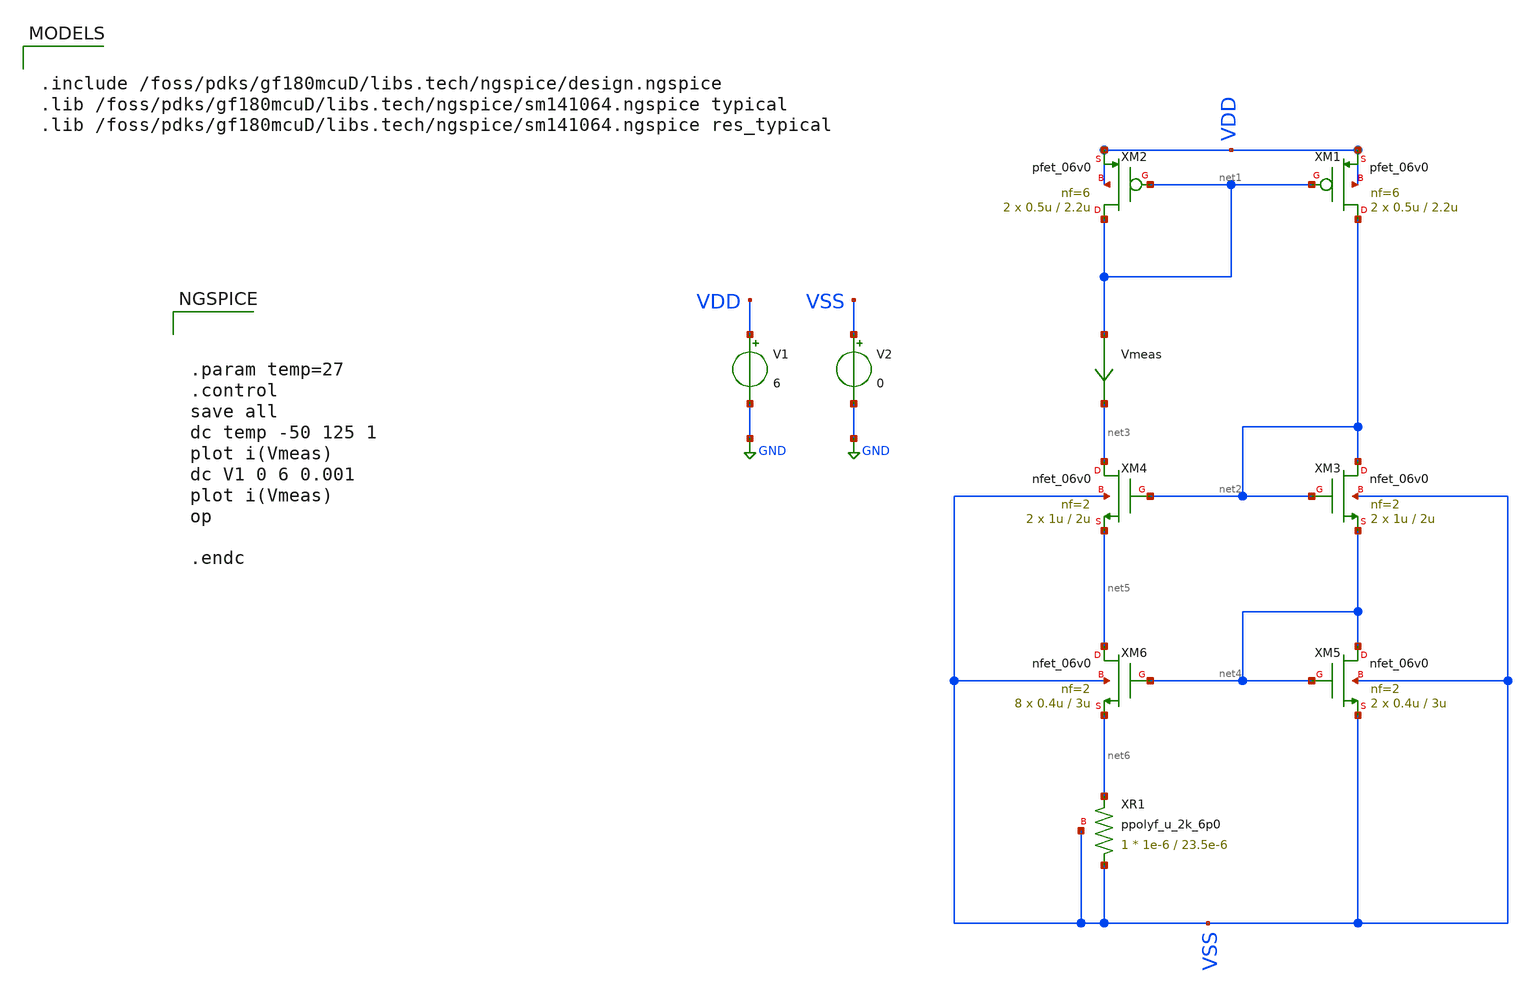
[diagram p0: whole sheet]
** sch_path: Learning/single_ended_amplifiers/VA001_series/Design_and_Analysis_of_Two-Stage_CMOS_Operational_Amplifier_for_Fluorescence_Signal_Processing_gf180mcu_6V/transcondutance/tb.sch
**.subckt tb
XM1 net2 net1 VDD VDD pfet_06v0 L=2.2u W=0.5u nf=6 ad='int((nf+1)/2) * W/nf * 0.18u' as='int((nf+2)/2) * W/nf * 0.18u'
+ pd='2*int((nf+1)/2) * (W/nf + 0.18u)' ps='2*int((nf+2)/2) * (W/nf + 0.18u)' nrd='0.18u / W' nrs='0.18u / W'
+ sa=0 sb=0 sd=0 m=2
XM2 net1 net1 VDD VDD pfet_06v0 L=2.2u W=0.5u nf=6 ad='int((nf+1)/2) * W/nf * 0.18u' as='int((nf+2)/2) * W/nf * 0.18u'
+ pd='2*int((nf+1)/2) * (W/nf + 0.18u)' ps='2*int((nf+2)/2) * (W/nf + 0.18u)' nrd='0.18u / W' nrs='0.18u / W'
+ sa=0 sb=0 sd=0 m=2
Vmeas net1 net3 0
.save i(vmeas)
V1 VDD GND 6
V2 VSS GND 0
XM3 net2 net2 net4 VSS nfet_06v0 L=2u W=1u nf=2 ad='int((nf+1)/2) * W/nf * 0.18u' as='int((nf+2)/2) * W/nf * 0.18u'
+ pd='2*int((nf+1)/2) * (W/nf + 0.18u)' ps='2*int((nf+2)/2) * (W/nf + 0.18u)' nrd='0.18u / W' nrs='0.18u / W'
+ sa=0 sb=0 sd=0 m=2
XM4 net3 net2 net5 VSS nfet_06v0 L=2u W=1u nf=2 ad='int((nf+1)/2) * W/nf * 0.18u' as='int((nf+2)/2) * W/nf * 0.18u'
+ pd='2*int((nf+1)/2) * (W/nf + 0.18u)' ps='2*int((nf+2)/2) * (W/nf + 0.18u)' nrd='0.18u / W' nrs='0.18u / W'
+ sa=0 sb=0 sd=0 m=2
XM6 net5 net4 net6 VSS nfet_06v0 L=3u W=0.4u nf=2 ad='int((nf+1)/2) * W/nf * 0.18u' as='int((nf+2)/2) * W/nf * 0.18u'
+ pd='2*int((nf+1)/2) * (W/nf + 0.18u)' ps='2*int((nf+2)/2) * (W/nf + 0.18u)' nrd='0.18u / W' nrs='0.18u / W'
+ sa=0 sb=0 sd=0 m=8
XR1 VSS net6 VSS ppolyf_u_2k_6p0 r_width=1e-6 r_length=23.5e-6 m=1
XM5 net4 net4 VSS VSS nfet_06v0 L=3u W=0.4u nf=2 ad='int((nf+1)/2) * W/nf * 0.18u' as='int((nf+2)/2) * W/nf * 0.18u'
+ pd='2*int((nf+1)/2) * (W/nf + 0.18u)' ps='2*int((nf+2)/2) * (W/nf + 0.18u)' nrd='0.18u / W' nrs='0.18u / W'
+ sa=0 sb=0 sd=0 m=2
**** begin user architecture code

.include /foss/pdks/gf180mcuD/libs.tech/ngspice/design.ngspice
.lib /foss/pdks/gf180mcuD/libs.tech/ngspice/sm141064.ngspice typical
.lib /foss/pdks/gf180mcuD/libs.tech/ngspice/sm141064.ngspice res_typical

**** end user architecture code
**.ends
.GLOBAL GND
**** begin user architecture code



.param temp=27
.control
save all
dc temp -50 125 1
plot i(Vmeas)
dc V1 0 6 0.001
plot i(Vmeas)
op

.endc


**** end user architecture code
.end
